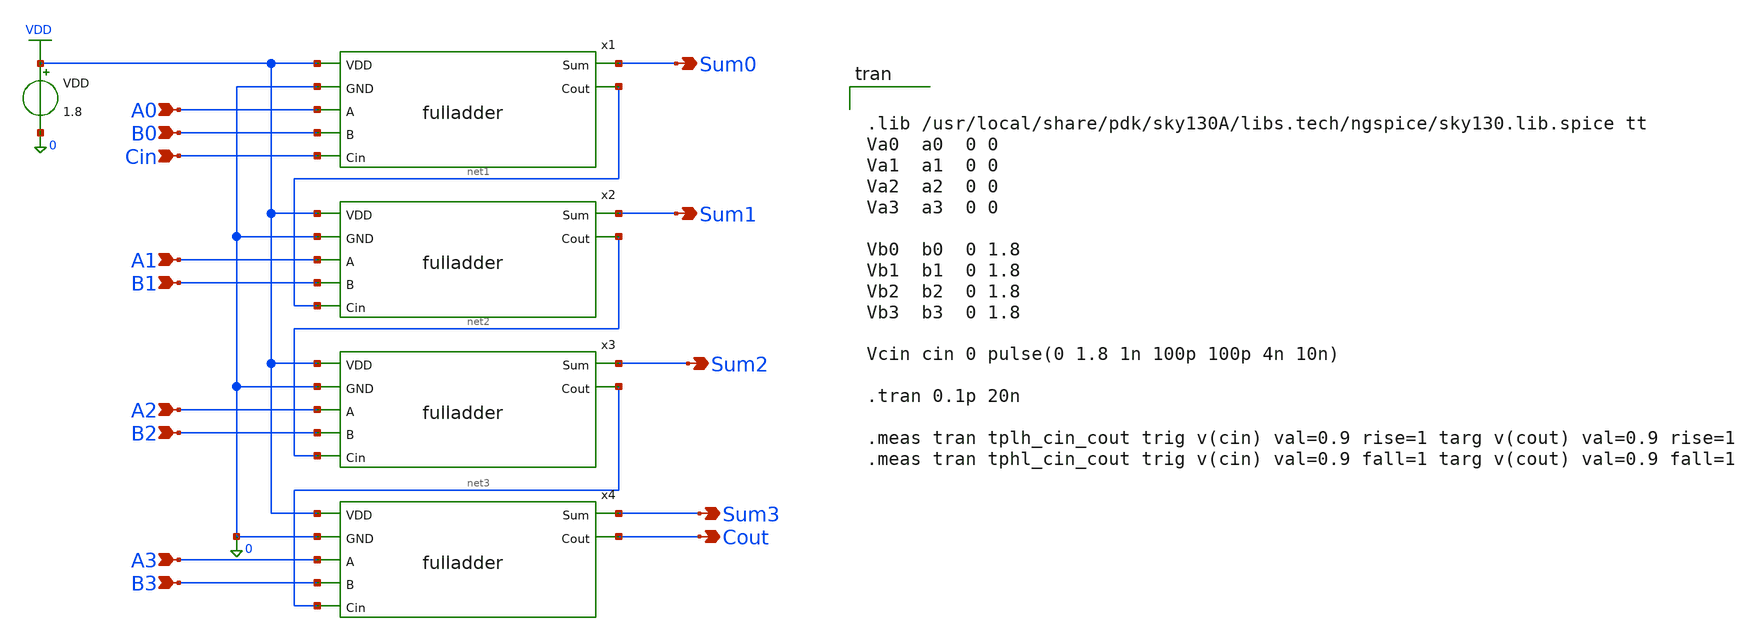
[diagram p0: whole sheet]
** sch_path: static_cmos/testbench/fa4_tb_delay.sch
**.subckt fa4_tb_delay Sum0 Sum1 Sum2 Sum3 Cout A0 B0 Cin A1 B1 B2 A2 B3 A3
*.opin Sum0
*.opin Sum1
*.opin Sum2
*.opin Sum3
*.opin Cout
*.ipin A0
*.ipin B0
*.ipin Cin
*.ipin A1
*.ipin B1
*.ipin B2
*.ipin A2
*.ipin B3
*.ipin A3
x1 VDD 0 Sum0 A0 B0 Cin net1 fulladder
x2 VDD 0 Sum1 A1 B1 net1 net2 fulladder
x3 VDD 0 Sum2 A2 B2 net2 net3 fulladder
x4 VDD 0 Sum3 A3 B3 net3 Cout fulladder
VDD VDD 0 1.8
**** begin user architecture code


.lib /usr/local/share/pdk/sky130A/libs.tech/ngspice/sky130.lib.spice tt
Va0  a0  0 0
Va1  a1  0 0
Va2  a2  0 0
Va3  a3  0 0

Vb0  b0  0 1.8
Vb1  b1  0 1.8
Vb2  b2  0 1.8
Vb3  b3  0 1.8

Vcin cin 0 pulse(0 1.8 1n 100p 100p 4n 10n)

.tran 0.1p 20n

.meas tran tplh_cin_cout trig v(cin) val=0.9 rise=1 targ v(cout) val=0.9 rise=1
.meas tran tphl_cin_cout trig v(cin) val=0.9 fall=1 targ v(cout) val=0.9 fall=1


**** end user architecture code
**.ends
.GLOBAL VDD
.end
